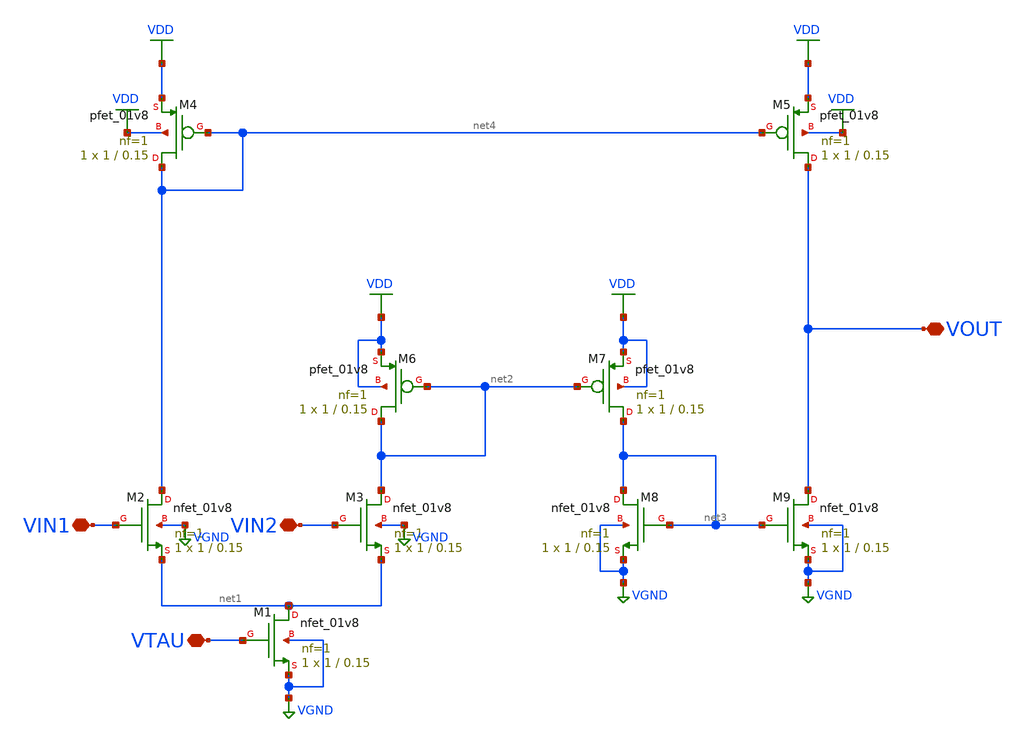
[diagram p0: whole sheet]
** sch_path: project2/diff_amp/diff_amp.sch
**.subckt diff_amp VOUT VIN1 VIN2 VTAU
*.iopin VOUT
*.iopin VIN1
*.iopin VIN2
*.iopin VTAU
XM1 net1 VTAU VGND VGND sky130_fd_pr__nfet_01v8 L=0.15 W=1 nf=1 ad='int((nf+1)/2) * W/nf * 0.29' as='int((nf+2)/2) * W/nf * 0.29'
+ pd='2*int((nf+1)/2) * (W/nf + 0.29)' ps='2*int((nf+2)/2) * (W/nf + 0.29)' nrd='0.29 / W' nrs='0.29 / W'
+ sa=0 sb=0 sd=0 mult=1 m=1
XM2 net4 VIN1 net1 VGND sky130_fd_pr__nfet_01v8 L=0.15 W=1 nf=1 ad='int((nf+1)/2) * W/nf * 0.29' as='int((nf+2)/2) * W/nf * 0.29'
+ pd='2*int((nf+1)/2) * (W/nf + 0.29)' ps='2*int((nf+2)/2) * (W/nf + 0.29)' nrd='0.29 / W' nrs='0.29 / W'
+ sa=0 sb=0 sd=0 mult=1 m=1
XM3 net2 VIN2 net1 VGND sky130_fd_pr__nfet_01v8 L=0.15 W=1 nf=1 ad='int((nf+1)/2) * W/nf * 0.29' as='int((nf+2)/2) * W/nf * 0.29'
+ pd='2*int((nf+1)/2) * (W/nf + 0.29)' ps='2*int((nf+2)/2) * (W/nf + 0.29)' nrd='0.29 / W' nrs='0.29 / W'
+ sa=0 sb=0 sd=0 mult=1 m=1
XM4 net4 net4 VDD VDD sky130_fd_pr__pfet_01v8 L=0.15 W=1 nf=1 ad='int((nf+1)/2) * W/nf * 0.29' as='int((nf+2)/2) * W/nf * 0.29'
+ pd='2*int((nf+1)/2) * (W/nf + 0.29)' ps='2*int((nf+2)/2) * (W/nf + 0.29)' nrd='0.29 / W' nrs='0.29 / W'
+ sa=0 sb=0 sd=0 mult=1 m=1
XM5 VOUT net4 VDD VDD sky130_fd_pr__pfet_01v8 L=0.15 W=1 nf=1 ad='int((nf+1)/2) * W/nf * 0.29' as='int((nf+2)/2) * W/nf * 0.29'
+ pd='2*int((nf+1)/2) * (W/nf + 0.29)' ps='2*int((nf+2)/2) * (W/nf + 0.29)' nrd='0.29 / W' nrs='0.29 / W'
+ sa=0 sb=0 sd=0 mult=1 m=1
XM6 net2 net2 VDD VDD sky130_fd_pr__pfet_01v8 L=0.15 W=1 nf=1 ad='int((nf+1)/2) * W/nf * 0.29' as='int((nf+2)/2) * W/nf * 0.29'
+ pd='2*int((nf+1)/2) * (W/nf + 0.29)' ps='2*int((nf+2)/2) * (W/nf + 0.29)' nrd='0.29 / W' nrs='0.29 / W'
+ sa=0 sb=0 sd=0 mult=1 m=1
XM7 net3 net2 VDD VDD sky130_fd_pr__pfet_01v8 L=0.15 W=1 nf=1 ad='int((nf+1)/2) * W/nf * 0.29' as='int((nf+2)/2) * W/nf * 0.29'
+ pd='2*int((nf+1)/2) * (W/nf + 0.29)' ps='2*int((nf+2)/2) * (W/nf + 0.29)' nrd='0.29 / W' nrs='0.29 / W'
+ sa=0 sb=0 sd=0 mult=1 m=1
XM8 net3 net3 VGND VGND sky130_fd_pr__nfet_01v8 L=0.15 W=1 nf=1 ad='int((nf+1)/2) * W/nf * 0.29' as='int((nf+2)/2) * W/nf * 0.29'
+ pd='2*int((nf+1)/2) * (W/nf + 0.29)' ps='2*int((nf+2)/2) * (W/nf + 0.29)' nrd='0.29 / W' nrs='0.29 / W'
+ sa=0 sb=0 sd=0 mult=1 m=1
XM9 VOUT net3 VGND VGND sky130_fd_pr__nfet_01v8 L=0.15 W=1 nf=1 ad='int((nf+1)/2) * W/nf * 0.29' as='int((nf+2)/2) * W/nf * 0.29'
+ pd='2*int((nf+1)/2) * (W/nf + 0.29)' ps='2*int((nf+2)/2) * (W/nf + 0.29)' nrd='0.29 / W' nrs='0.29 / W'
+ sa=0 sb=0 sd=0 mult=1 m=1
**.ends
.GLOBAL VGND
.GLOBAL VDD
.end
